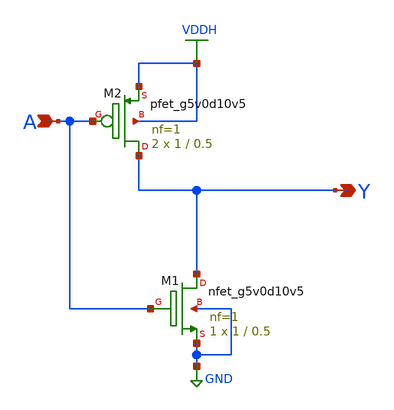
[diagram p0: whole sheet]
** sch_path: Ene_Thompson/inv.sch
**.subckt inv A Y
*.ipin A
*.opin Y
XM1 Y A GND GND sky130_fd_pr__nfet_g5v0d10v5 L=0.5 W=1 nf=1 ad='int((nf+1)/2) * W/nf * 0.29' as='int((nf+2)/2) * W/nf * 0.29'
+ pd='2*int((nf+1)/2) * (W/nf + 0.29)' ps='2*int((nf+2)/2) * (W/nf + 0.29)' nrd='0.29 / W' nrs='0.29 / W'
+ sa=0 sb=0 sd=0 mult=1 m=1
XM2 Y A VDDH VDDH sky130_fd_pr__pfet_g5v0d10v5 L=0.5 W=1 nf=1 ad='int((nf+1)/2) * W/nf * 0.29' as='int((nf+2)/2) * W/nf * 0.29'
+ pd='2*int((nf+1)/2) * (W/nf + 0.29)' ps='2*int((nf+2)/2) * (W/nf + 0.29)' nrd='0.29 / W' nrs='0.29 / W'
+ sa=0 sb=0 sd=0 mult=2 m=2
**.ends
.GLOBAL VDDH
.GLOBAL GND
.end
